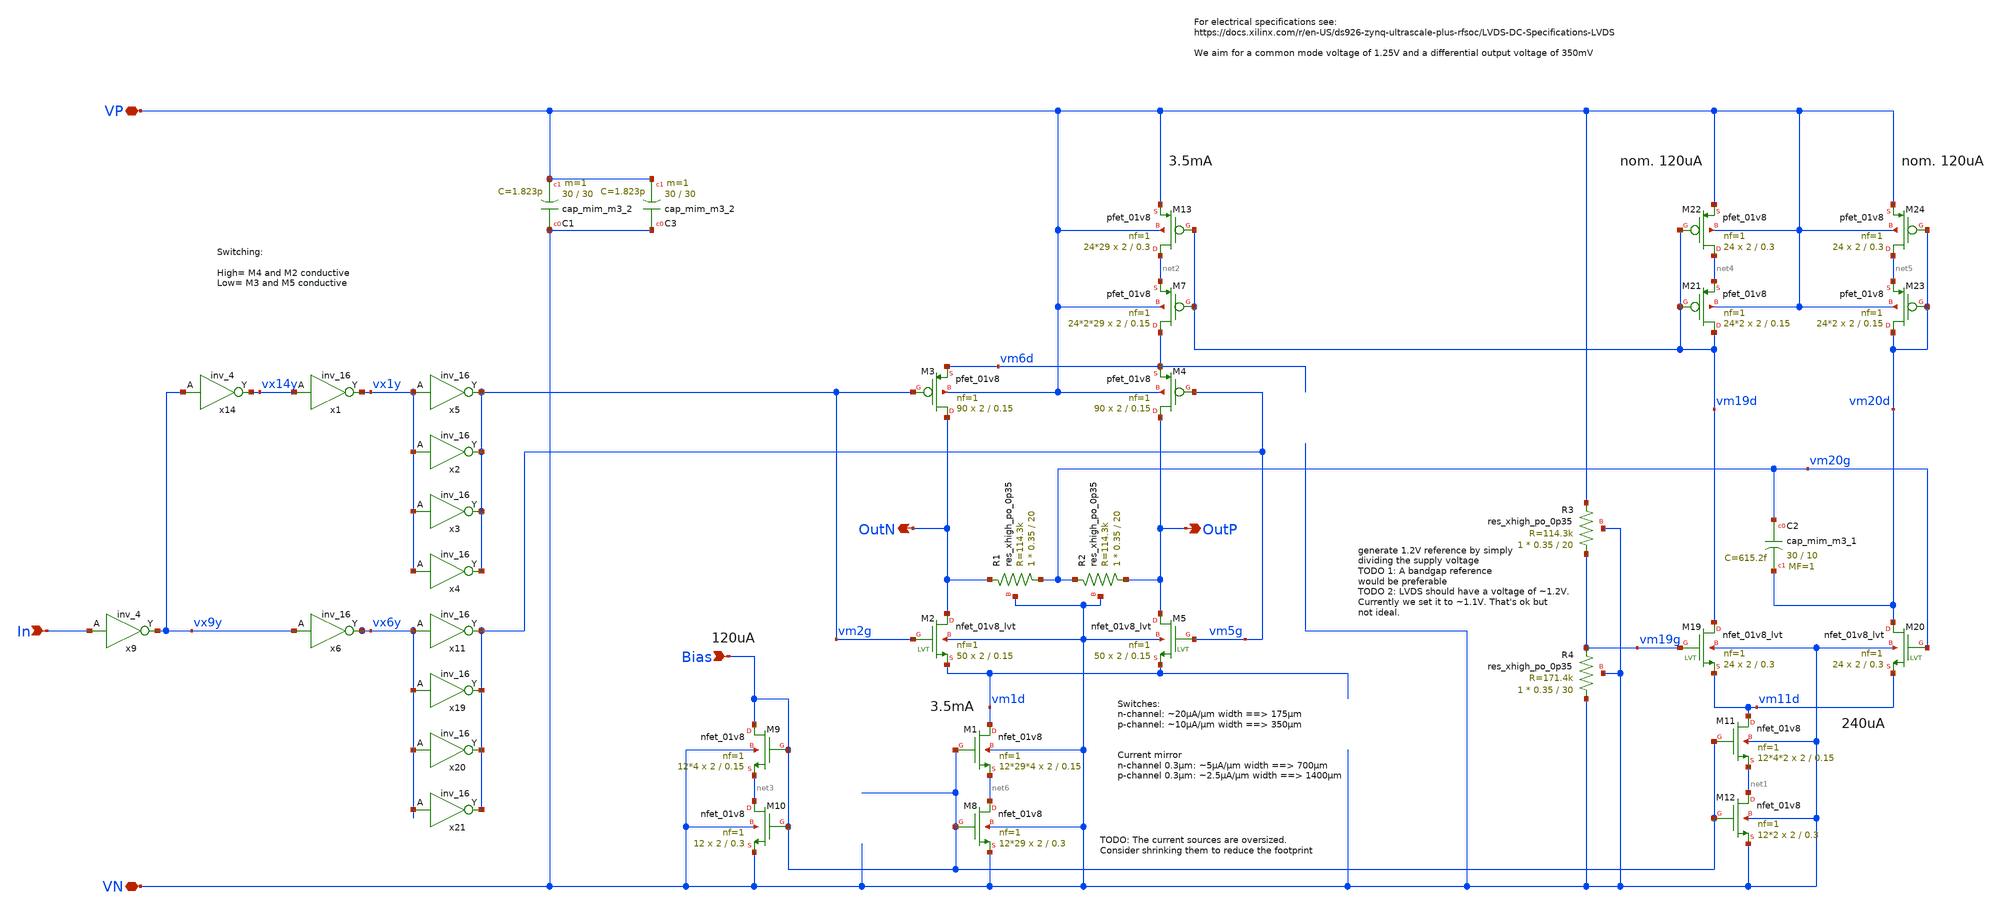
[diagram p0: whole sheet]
** sch_path: xschem/lvds/transmitter.sch
**.subckt transmitter In VP OutP VN OutN Bias
*.ipin In
*.iopin VP
*.opin OutP
*.iopin VN
*.opin OutN
*.ipin Bias
XR1 vm20g OutN VN sky130_fd_pr__res_xhigh_po_0p35 L=20 mult=1 m=1
XM3 OutN vm2g vm6d VP sky130_fd_pr__pfet_01v8 L=0.15 W=2 nf=1 ad='int((nf+1)/2) * W/nf * 0.29' as='int((nf+2)/2) * W/nf * 0.29'
+ pd='2*int((nf+1)/2) * (W/nf + 0.29)' ps='2*int((nf+2)/2) * (W/nf + 0.29)' nrd='0.29 / W' nrs='0.29 / W'
+ sa=0 sb=0 sd=0 mult=90 m=90
XM4 OutP vm5g vm6d VP sky130_fd_pr__pfet_01v8 L=0.15 W=2 nf=1 ad='int((nf+1)/2) * W/nf * 0.29' as='int((nf+2)/2) * W/nf * 0.29'
+ pd='2*int((nf+1)/2) * (W/nf + 0.29)' ps='2*int((nf+2)/2) * (W/nf + 0.29)' nrd='0.29 / W' nrs='0.29 / W'
+ sa=0 sb=0 sd=0 mult=90 m=90
XM7 vm6d vm19d net2 VP sky130_fd_pr__pfet_01v8 L=0.15 W=2 nf=1 ad='int((nf+1)/2) * W/nf * 0.29' as='int((nf+2)/2) * W/nf * 0.29'
+ pd='2*int((nf+1)/2) * (W/nf + 0.29)' ps='2*int((nf+2)/2) * (W/nf + 0.29)' nrd='0.29 / W' nrs='0.29 / W'
+ sa=0 sb=0 sd=0 mult=24*2*29 m=24*2*29
XR2 OutP vm20g VN sky130_fd_pr__res_xhigh_po_0p35 L=20 mult=1 m=1
XR3 vm19g VP VN sky130_fd_pr__res_xhigh_po_0p35 L=20 mult=1 m=1
XM9 Bias Bias net3 VN sky130_fd_pr__nfet_01v8 L=0.15 W=2 nf=1 ad='int((nf+1)/2) * W/nf * 0.29' as='int((nf+2)/2) * W/nf * 0.29'
+ pd='2*int((nf+1)/2) * (W/nf + 0.29)' ps='2*int((nf+2)/2) * (W/nf + 0.29)' nrd='0.29 / W' nrs='0.29 / W'
+ sa=0 sb=0 sd=0 mult=12*4 m=12*4
XM10 net3 Bias VN VN sky130_fd_pr__nfet_01v8 L=0.3 W=2 nf=1 ad='int((nf+1)/2) * W/nf * 0.29' as='int((nf+2)/2) * W/nf * 0.29'
+ pd='2*int((nf+1)/2) * (W/nf + 0.29)' ps='2*int((nf+2)/2) * (W/nf + 0.29)' nrd='0.29 / W' nrs='0.29 / W'
+ sa=0 sb=0 sd=0 mult=12 m=12
XR4 VN vm19g VN sky130_fd_pr__res_xhigh_po_0p35 L=30 mult=1 m=1
XM11 vm11d Bias net1 VN sky130_fd_pr__nfet_01v8 L=0.15 W=2 nf=1 ad='int((nf+1)/2) * W/nf * 0.29' as='int((nf+2)/2) * W/nf * 0.29'
+ pd='2*int((nf+1)/2) * (W/nf + 0.29)' ps='2*int((nf+2)/2) * (W/nf + 0.29)' nrd='0.29 / W' nrs='0.29 / W'
+ sa=0 sb=0 sd=0 mult=12*4*2 m=12*4*2
XM12 net1 Bias VN VN sky130_fd_pr__nfet_01v8 L=0.3 W=2 nf=1 ad='int((nf+1)/2) * W/nf * 0.29' as='int((nf+2)/2) * W/nf * 0.29'
+ pd='2*int((nf+1)/2) * (W/nf + 0.29)' ps='2*int((nf+2)/2) * (W/nf + 0.29)' nrd='0.29 / W' nrs='0.29 / W'
+ sa=0 sb=0 sd=0 mult=12*2 m=12*2
XM13 net2 vm19d VP VP sky130_fd_pr__pfet_01v8 L=0.3 W=2 nf=1 ad='int((nf+1)/2) * W/nf * 0.29' as='int((nf+2)/2) * W/nf * 0.29'
+ pd='2*int((nf+1)/2) * (W/nf + 0.29)' ps='2*int((nf+2)/2) * (W/nf + 0.29)' nrd='0.29 / W' nrs='0.29 / W'
+ sa=0 sb=0 sd=0 mult=24*29 m=24*29
XM19 vm19d vm19g vm11d VN sky130_fd_pr__nfet_01v8_lvt L=0.3 W=2 nf=1 ad='int((nf+1)/2) * W/nf * 0.29'
+ as='int((nf+2)/2) * W/nf * 0.29' pd='2*int((nf+1)/2) * (W/nf + 0.29)' ps='2*int((nf+2)/2) * (W/nf + 0.29)'
+ nrd='0.29 / W' nrs='0.29 / W' sa=0 sb=0 sd=0 mult=24 m=24
XM20 vm20d vm20g vm11d VN sky130_fd_pr__nfet_01v8_lvt L=0.3 W=2 nf=1 ad='int((nf+1)/2) * W/nf * 0.29'
+ as='int((nf+2)/2) * W/nf * 0.29' pd='2*int((nf+1)/2) * (W/nf + 0.29)' ps='2*int((nf+2)/2) * (W/nf + 0.29)'
+ nrd='0.29 / W' nrs='0.29 / W' sa=0 sb=0 sd=0 mult=24 m=24
XM21 vm19d vm19d net4 VP sky130_fd_pr__pfet_01v8 L=0.15 W=2 nf=1 ad='int((nf+1)/2) * W/nf * 0.29' as='int((nf+2)/2) * W/nf * 0.29'
+ pd='2*int((nf+1)/2) * (W/nf + 0.29)' ps='2*int((nf+2)/2) * (W/nf + 0.29)' nrd='0.29 / W' nrs='0.29 / W'
+ sa=0 sb=0 sd=0 mult=24*2 m=24*2
XM22 net4 vm19d VP VP sky130_fd_pr__pfet_01v8 L=0.3 W=2 nf=1 ad='int((nf+1)/2) * W/nf * 0.29' as='int((nf+2)/2) * W/nf * 0.29'
+ pd='2*int((nf+1)/2) * (W/nf + 0.29)' ps='2*int((nf+2)/2) * (W/nf + 0.29)' nrd='0.29 / W' nrs='0.29 / W'
+ sa=0 sb=0 sd=0 mult=24 m=24
XM24 net5 vm20d VP VP sky130_fd_pr__pfet_01v8 L=0.3 W=2 nf=1 ad='int((nf+1)/2) * W/nf * 0.29' as='int((nf+2)/2) * W/nf * 0.29'
+ pd='2*int((nf+1)/2) * (W/nf + 0.29)' ps='2*int((nf+2)/2) * (W/nf + 0.29)' nrd='0.29 / W' nrs='0.29 / W'
+ sa=0 sb=0 sd=0 mult=24 m=24
XC2 vm20g vm20d sky130_fd_pr__cap_mim_m3_1 W=30 L=10 MF=1 m=1
x5 vx1y VN VN VP VP vm2g sky130_fd_sc_hs__inv_16
XM23 vm20d vm20d net5 VP sky130_fd_pr__pfet_01v8 L=0.15 W=2 nf=1 ad='int((nf+1)/2) * W/nf * 0.29' as='int((nf+2)/2) * W/nf * 0.29'
+ pd='2*int((nf+1)/2) * (W/nf + 0.29)' ps='2*int((nf+2)/2) * (W/nf + 0.29)' nrd='0.29 / W' nrs='0.29 / W'
+ sa=0 sb=0 sd=0 mult=24*2 m=24*2
x9 In VN VN VP VP vx9y sky130_fd_sc_hs__inv_4
x2 vx1y VN VN VP VP vm2g sky130_fd_sc_hs__inv_16
x3 vx1y VN VN VP VP vm2g sky130_fd_sc_hs__inv_16
x4 vx1y VN VN VP VP vm2g sky130_fd_sc_hs__inv_16
XM1 vm1d Bias net6 VN sky130_fd_pr__nfet_01v8 L=0.15 W=2 nf=1 ad='int((nf+1)/2) * W/nf * 0.29' as='int((nf+2)/2) * W/nf * 0.29'
+ pd='2*int((nf+1)/2) * (W/nf + 0.29)' ps='2*int((nf+2)/2) * (W/nf + 0.29)' nrd='0.29 / W' nrs='0.29 / W'
+ sa=0 sb=0 sd=0 mult=12*29*4 m=12*29*4
XM8 net6 Bias VN VN sky130_fd_pr__nfet_01v8 L=0.3 W=2 nf=1 ad='int((nf+1)/2) * W/nf * 0.29' as='int((nf+2)/2) * W/nf * 0.29'
+ pd='2*int((nf+1)/2) * (W/nf + 0.29)' ps='2*int((nf+2)/2) * (W/nf + 0.29)' nrd='0.29 / W' nrs='0.29 / W'
+ sa=0 sb=0 sd=0 mult=12*29 m=12*29
x11 vx6y VN VN VP VP vm5g sky130_fd_sc_hs__inv_16
x19 vx6y VN VN VP VP vm5g sky130_fd_sc_hs__inv_16
x20 vx6y VN VN VP VP vm5g sky130_fd_sc_hs__inv_16
x21 vx6y VN VN VP VP vm5g sky130_fd_sc_hs__inv_16
x14 vx9y VN VN VP VP vx14y sky130_fd_sc_hs__inv_4
x1 vx14y VN VN VP VP vx1y sky130_fd_sc_hs__inv_16
x6 vx9y VN VN VP VP vx6y sky130_fd_sc_hs__inv_16
XM2 OutN vm2g vm1d VN sky130_fd_pr__nfet_01v8_lvt L=0.15 W=2 nf=1 ad='int((nf+1)/2) * W/nf * 0.29' as='int((nf+2)/2) * W/nf * 0.29'
+ pd='2*int((nf+1)/2) * (W/nf + 0.29)' ps='2*int((nf+2)/2) * (W/nf + 0.29)' nrd='0.29 / W' nrs='0.29 / W'
+ sa=0 sb=0 sd=0 mult=50 m=50
XM5 OutP vm5g vm1d VN sky130_fd_pr__nfet_01v8_lvt L=0.15 W=2 nf=1 ad='int((nf+1)/2) * W/nf * 0.29' as='int((nf+2)/2) * W/nf * 0.29'
+ pd='2*int((nf+1)/2) * (W/nf + 0.29)' ps='2*int((nf+2)/2) * (W/nf + 0.29)' nrd='0.29 / W' nrs='0.29 / W'
+ sa=0 sb=0 sd=0 mult=50 m=50
XC1 VN VP sky130_fd_pr__cap_mim_m3_2 W=30 L=30 MF=1 m=1
XC3 VN VP sky130_fd_pr__cap_mim_m3_2 W=30 L=30 MF=1 m=1
**** begin user architecture code


.include /usr/local/share/pdk/sky130B/libs.ref/sky130_fd_sc_hs/spice/sky130_fd_sc_hs.spice


**** end user architecture code
**.ends
.end
